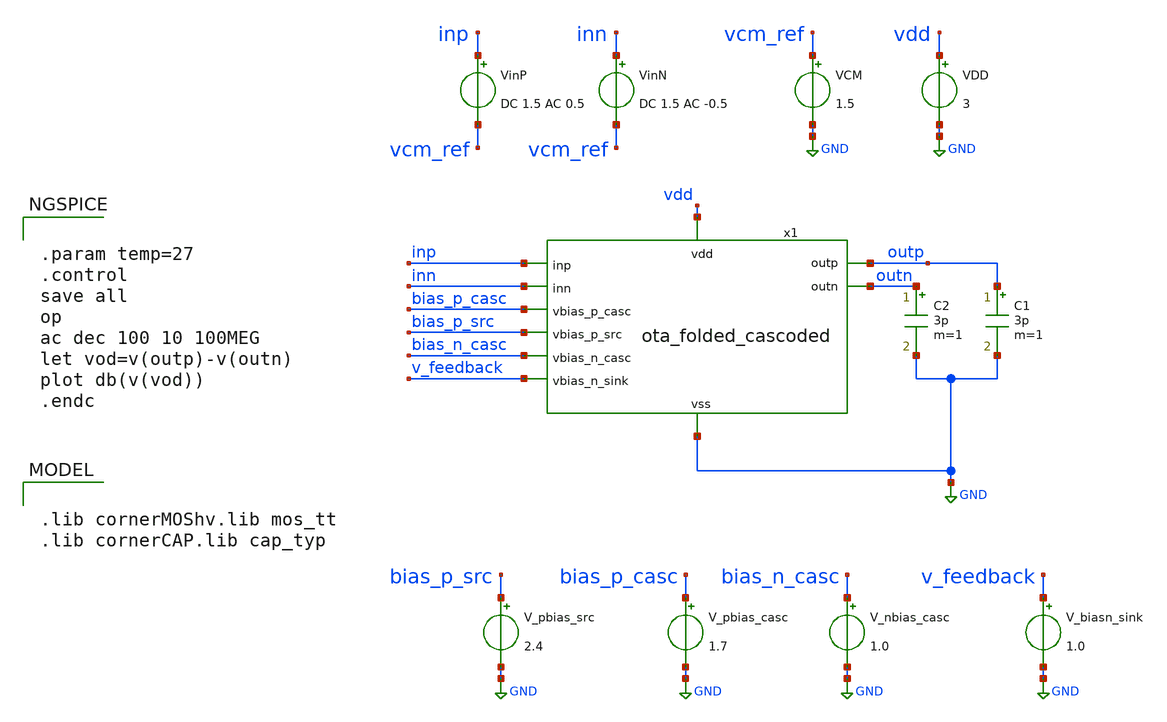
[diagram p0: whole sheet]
** sch_path: 3_real_circuits/ota_folded_cascoded_ac.sch
**.subckt ota_folded_cascoded_ac
VCM vcm_ref GND 1.5
VinP inp vcm_ref DC 1.5 AC 0.5
VinN inn vcm_ref DC 1.5 AC -0.5
x1 inp inn outp GND outn bias_p_casc bias_p_src bias_n_casc v_feedback vdd ota_folded_cascoded
VDD vdd GND 3
V_pbias_src bias_p_src GND 2.4
V_pbias_casc bias_p_casc GND 1.7
V_nbias_casc bias_n_casc GND 1.0
V_biasn_sink v_feedback GND 1.0
C1 outp GND 3p m=1
C2 outn GND 3p m=1
**** begin user architecture code


.param temp=27
.control
save all
op
ac dec 100 10 100MEG
let vod=v(outp)-v(outn)
plot db(v(vod))
.endc



.lib cornerMOShv.lib mos_tt
.lib cornerCAP.lib cap_typ

**** end user architecture code
**.ends

* expanding   symbol:  ota_folded_cascoded.sym # of pins=12
** sym_path: 3_real_circuits/ota_folded_cascoded.sym
** sch_path: 3_real_circuits/ota_folded_cascoded.sch
.subckt ota_folded_cascoded inp inn outp vss outn vbias_p_casc vbias_p_src vbias_n_casc vbias_n_sink
+ vdd
*.ipin inp
*.ipin inn
*.iopin vss
*.ipin vdd
*.opin outn
*.opin outp
*.ipin vbias_n_casc
*.ipin vbias_p_casc
*.ipin vbias_p_src
*.ipin vbias_n_sink
XM1 net5 inp net1 vss sg13_hv_nmos w=6.2u l=1u ng=1 m=1 mm_ok=1
XM10 net5 vbias_p_src vdd vdd sg13_hv_pmos w=7.05u l=1u ng=1 m=1 mm_ok=1
XM8 outn vbias_p_casc net5 vdd sg13_hv_pmos w=4.6u l=0.4u ng=1 m=1 mm_ok=1
XM11 net4 vbias_p_src vdd vdd sg13_hv_pmos w=7.05u l=1u ng=1 m=1 mm_ok=1
XM9 outp vbias_p_casc net4 vdd sg13_hv_pmos w=4.6u l=0.4u ng=1 m=1 mm_ok=1
XM7 outp vbias_n_casc net3 vss sg13_hv_nmos w=1u l=0.45u ng=1 m=1 mm_ok=1
XM5 net3 vbias_n_sink vss vss sg13_hv_nmos w=1.13u l=1u ng=1 m=1 mm_ok=1
XM4 net2 vbias_n_sink vss vss sg13_hv_nmos w=1.13u l=1u ng=1 m=1 mm_ok=1
XM6 outn vbias_n_casc net2 vss sg13_hv_nmos w=1u l=0.45u ng=1 m=1 mm_ok=1
XM2 net4 inn net1 vss sg13_hv_nmos w=6.2u l=1u ng=1 m=1 mm_ok=1
XM3 net1 vbias_n_sink vss vss sg13_hv_nmos w=3.25u l=1.5u ng=1 m=1 mm_ok=1
.ends

.GLOBAL GND
.end
